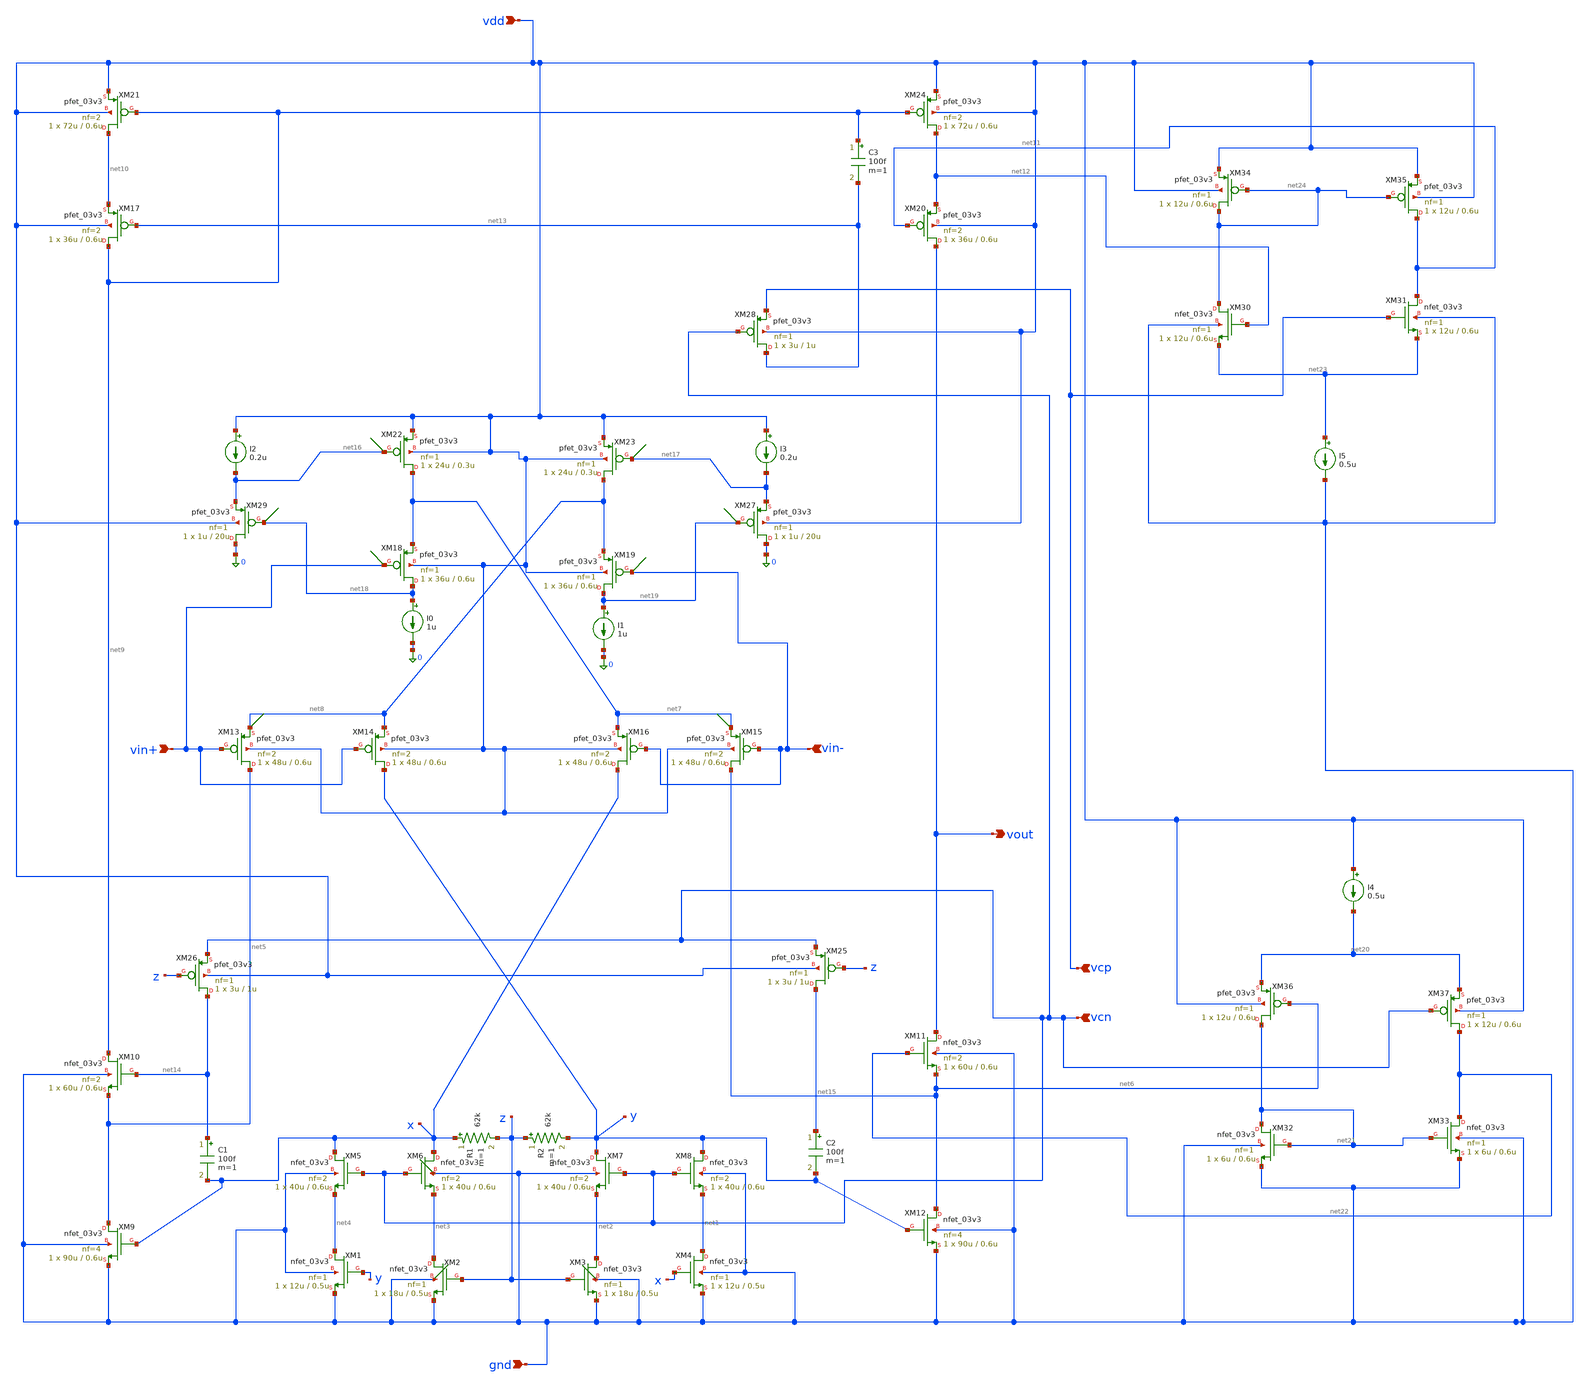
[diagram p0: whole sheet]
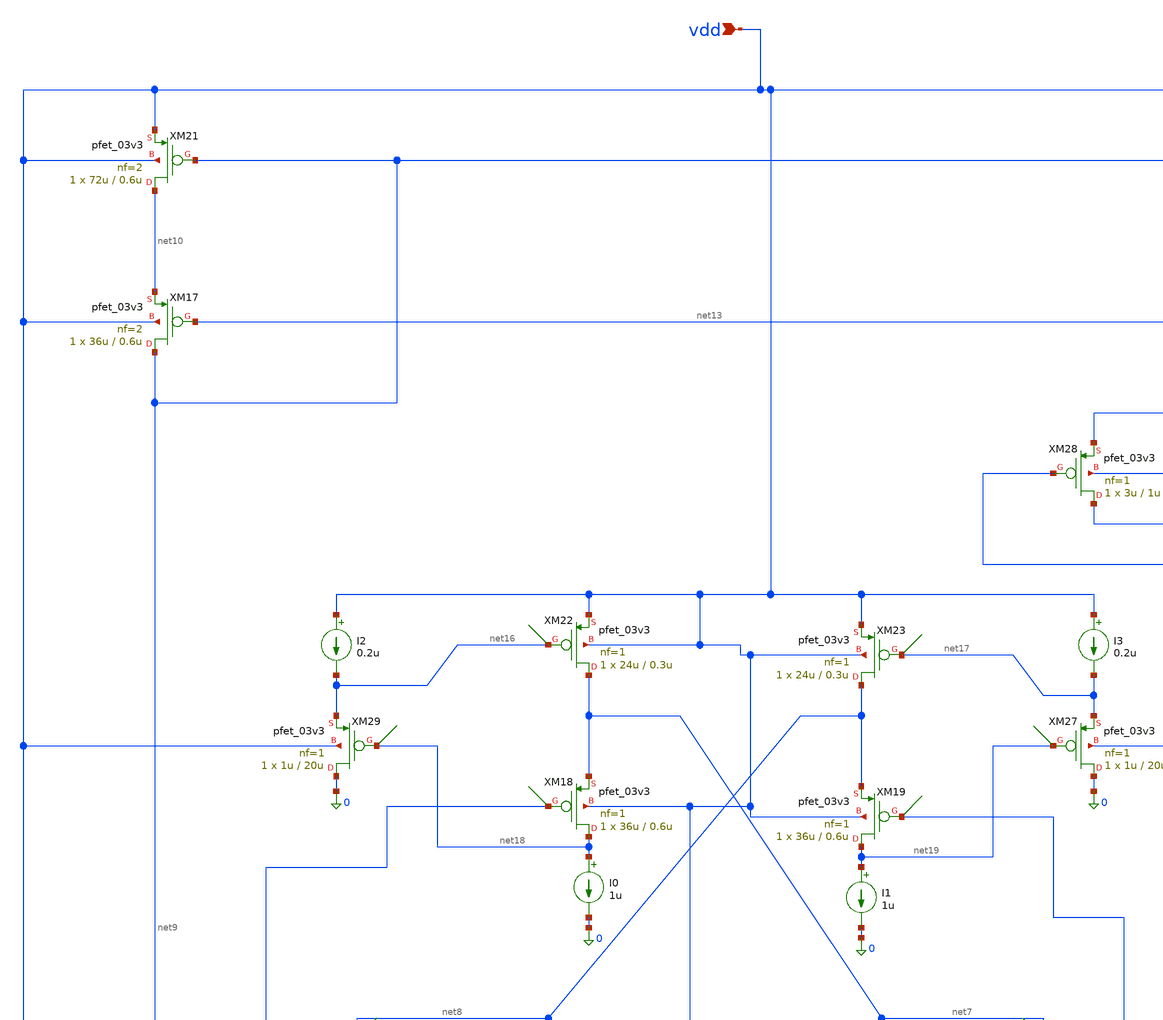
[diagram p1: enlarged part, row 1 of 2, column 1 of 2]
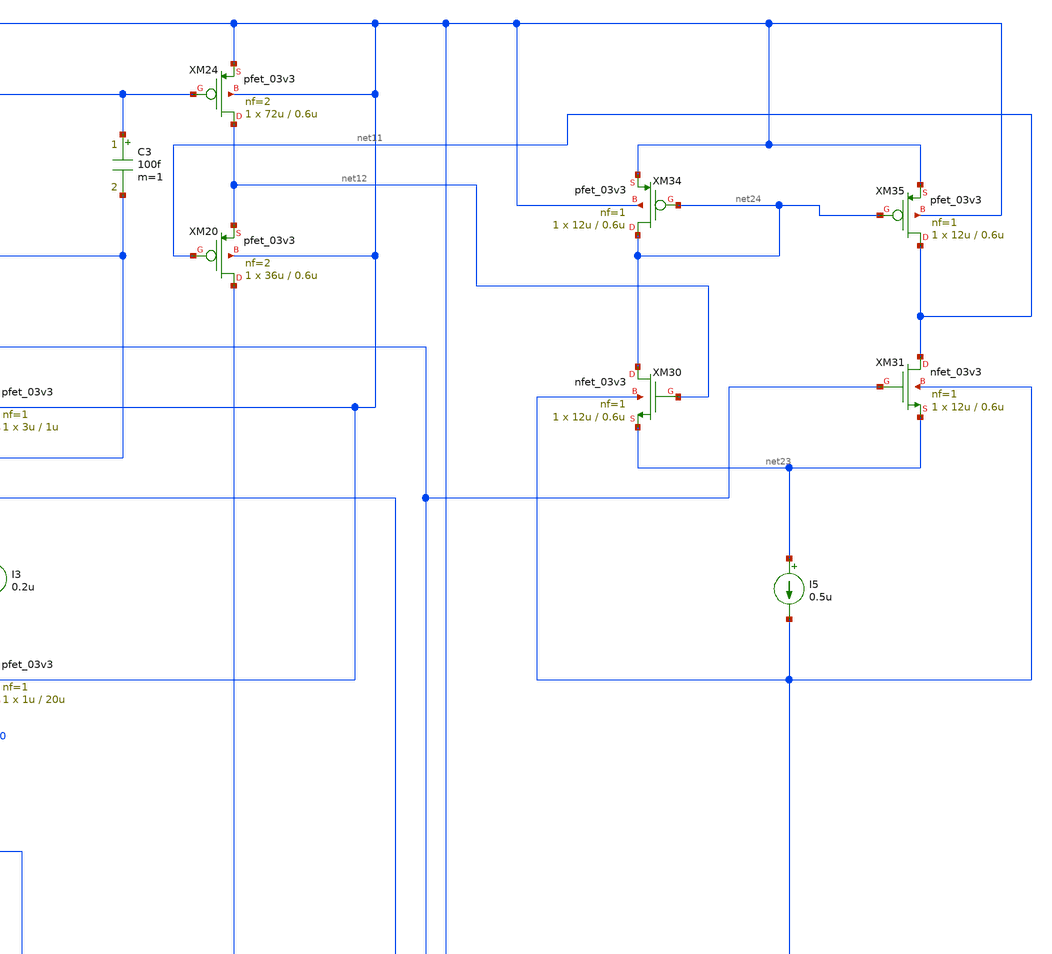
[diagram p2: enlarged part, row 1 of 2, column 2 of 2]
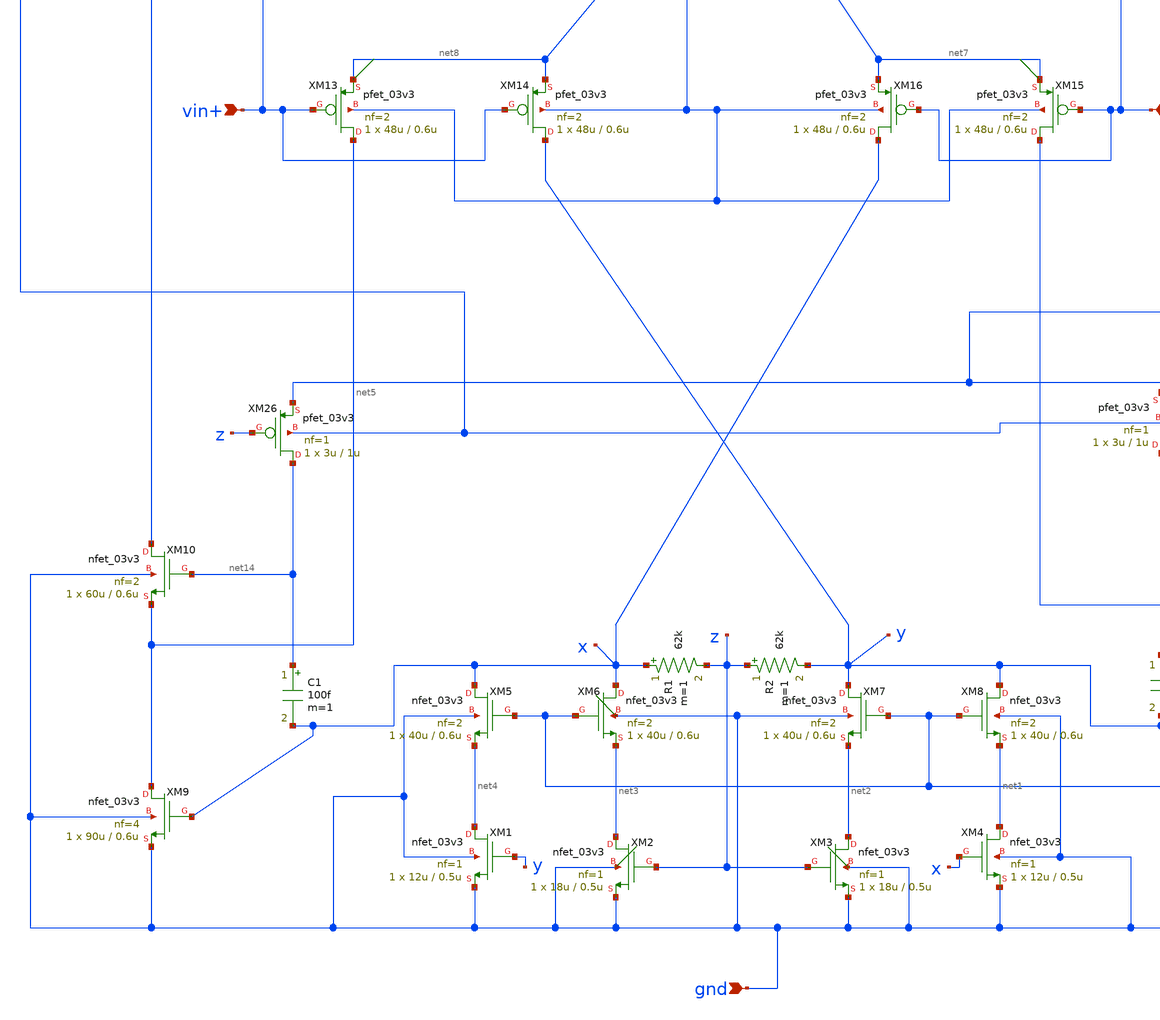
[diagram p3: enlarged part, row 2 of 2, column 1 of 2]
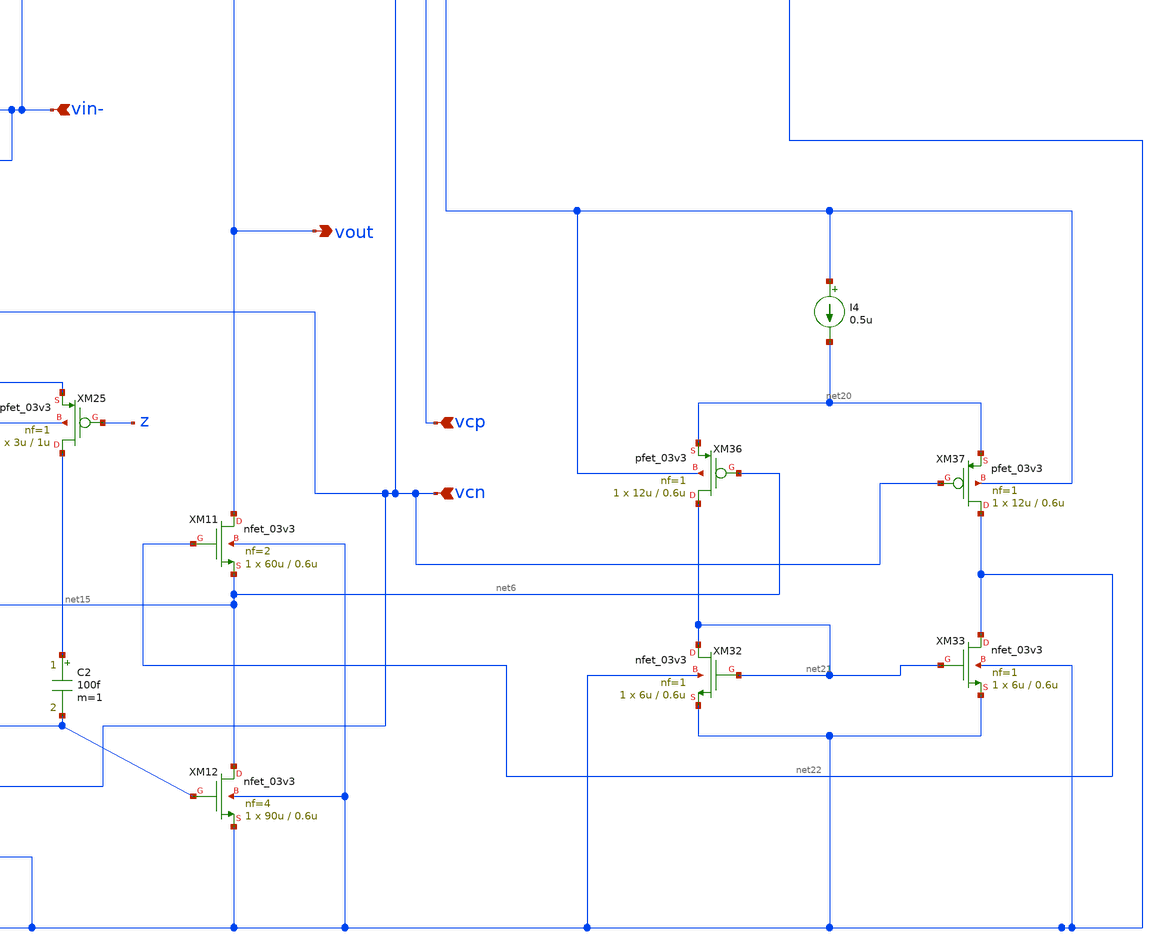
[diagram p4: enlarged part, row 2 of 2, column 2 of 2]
** sch_path: schematic/exp1.sch
**.subckt exp1 gnd vin+ vcp vcn vdd vin- vout
*.ipin gnd
*.ipin vin+
*.ipin vcp
*.ipin vcn
*.ipin vdd
*.ipin vin-
*.opin vout
XM1 net4 y gnd gnd nfet_03v3 L=0.5u W=12u nf=1 ad='int((nf+1)/2) * W/nf * 0.18u' as='int((nf+2)/2) * W/nf * 0.18u'
+ pd='2*int((nf+1)/2) * (W/nf + 0.18u)' ps='2*int((nf+2)/2) * (W/nf + 0.18u)' nrd='0.18u / W' nrs='0.18u / W'
+ sa=0 sb=0 sd=0 m=1
XM2 net3 z gnd gnd nfet_03v3 L=0.5u W=18u nf=1 ad='int((nf+1)/2) * W/nf * 0.18u' as='int((nf+2)/2) * W/nf * 0.18u'
+ pd='2*int((nf+1)/2) * (W/nf + 0.18u)' ps='2*int((nf+2)/2) * (W/nf + 0.18u)' nrd='0.18u / W' nrs='0.18u / W'
+ sa=0 sb=0 sd=0 m=1
XM3 net2 z gnd gnd nfet_03v3 L=0.5u W=18u nf=1 ad='int((nf+1)/2) * W/nf * 0.18u' as='int((nf+2)/2) * W/nf * 0.18u'
+ pd='2*int((nf+1)/2) * (W/nf + 0.18u)' ps='2*int((nf+2)/2) * (W/nf + 0.18u)' nrd='0.18u / W' nrs='0.18u / W'
+ sa=0 sb=0 sd=0 m=1
XM4 net1 x gnd gnd nfet_03v3 L=0.5u W=12u nf=1 ad='int((nf+1)/2) * W/nf * 0.18u' as='int((nf+2)/2) * W/nf * 0.18u'
+ pd='2*int((nf+1)/2) * (W/nf + 0.18u)' ps='2*int((nf+2)/2) * (W/nf + 0.18u)' nrd='0.18u / W' nrs='0.18u / W'
+ sa=0 sb=0 sd=0 m=1
XM5 x vcn net4 gnd nfet_03v3 L=0.6u W=40u nf=2 ad='int((nf+1)/2) * W/nf * 0.18u' as='int((nf+2)/2) * W/nf * 0.18u'
+ pd='2*int((nf+1)/2) * (W/nf + 0.18u)' ps='2*int((nf+2)/2) * (W/nf + 0.18u)' nrd='0.18u / W' nrs='0.18u / W'
+ sa=0 sb=0 sd=0 m=1
XM6 x vcn net3 gnd nfet_03v3 L=0.6u W=40u nf=2 ad='int((nf+1)/2) * W/nf * 0.18u' as='int((nf+2)/2) * W/nf * 0.18u'
+ pd='2*int((nf+1)/2) * (W/nf + 0.18u)' ps='2*int((nf+2)/2) * (W/nf + 0.18u)' nrd='0.18u / W' nrs='0.18u / W'
+ sa=0 sb=0 sd=0 m=1
XM7 y vcn net2 gnd nfet_03v3 L=0.6u W=40u nf=2 ad='int((nf+1)/2) * W/nf * 0.18u' as='int((nf+2)/2) * W/nf * 0.18u'
+ pd='2*int((nf+1)/2) * (W/nf + 0.18u)' ps='2*int((nf+2)/2) * (W/nf + 0.18u)' nrd='0.18u / W' nrs='0.18u / W'
+ sa=0 sb=0 sd=0 m=1
XM8 y vcn net1 gnd nfet_03v3 L=0.6u W=40u nf=2 ad='int((nf+1)/2) * W/nf * 0.18u' as='int((nf+2)/2) * W/nf * 0.18u'
+ pd='2*int((nf+1)/2) * (W/nf + 0.18u)' ps='2*int((nf+2)/2) * (W/nf + 0.18u)' nrd='0.18u / W' nrs='0.18u / W'
+ sa=0 sb=0 sd=0 m=1
XM9 net5 x gnd gnd nfet_03v3 L=0.6u W=90u nf=4 ad='int((nf+1)/2) * W/nf * 0.18u' as='int((nf+2)/2) * W/nf * 0.18u'
+ pd='2*int((nf+1)/2) * (W/nf + 0.18u)' ps='2*int((nf+2)/2) * (W/nf + 0.18u)' nrd='0.18u / W' nrs='0.18u / W'
+ sa=0 sb=0 sd=0 m=1
XM10 net9 net14 net5 gnd nfet_03v3 L=0.6u W=60u nf=2 ad='int((nf+1)/2) * W/nf * 0.18u' as='int((nf+2)/2) * W/nf * 0.18u'
+ pd='2*int((nf+1)/2) * (W/nf + 0.18u)' ps='2*int((nf+2)/2) * (W/nf + 0.18u)' nrd='0.18u / W' nrs='0.18u / W'
+ sa=0 sb=0 sd=0 m=1
XM11 vout net22 net6 gnd nfet_03v3 L=0.6u W=60u nf=2 ad='int((nf+1)/2) * W/nf * 0.18u' as='int((nf+2)/2) * W/nf * 0.18u'
+ pd='2*int((nf+1)/2) * (W/nf + 0.18u)' ps='2*int((nf+2)/2) * (W/nf + 0.18u)' nrd='0.18u / W' nrs='0.18u / W'
+ sa=0 sb=0 sd=0 m=1
XM12 net6 y gnd gnd nfet_03v3 L=0.6u W=90u nf=4 ad='int((nf+1)/2) * W/nf * 0.18u' as='int((nf+2)/2) * W/nf * 0.18u'
+ pd='2*int((nf+1)/2) * (W/nf + 0.18u)' ps='2*int((nf+2)/2) * (W/nf + 0.18u)' nrd='0.18u / W' nrs='0.18u / W'
+ sa=0 sb=0 sd=0 m=1
XM13 net5 vin+ net8 vdd pfet_03v3 L=0.6u W=48u nf=2 ad='int((nf+1)/2) * W/nf * 0.18u' as='int((nf+2)/2) * W/nf * 0.18u'
+ pd='2*int((nf+1)/2) * (W/nf + 0.18u)' ps='2*int((nf+2)/2) * (W/nf + 0.18u)' nrd='0.18u / W' nrs='0.18u / W'
+ sa=0 sb=0 sd=0 m=1
XM14 y vin+ net8 vdd pfet_03v3 L=0.6u W=48u nf=2 ad='int((nf+1)/2) * W/nf * 0.18u' as='int((nf+2)/2) * W/nf * 0.18u'
+ pd='2*int((nf+1)/2) * (W/nf + 0.18u)' ps='2*int((nf+2)/2) * (W/nf + 0.18u)' nrd='0.18u / W' nrs='0.18u / W'
+ sa=0 sb=0 sd=0 m=1
XM15 net6 vin- net7 vdd pfet_03v3 L=0.6u W=48u nf=2 ad='int((nf+1)/2) * W/nf * 0.18u' as='int((nf+2)/2) * W/nf * 0.18u'
+ pd='2*int((nf+1)/2) * (W/nf + 0.18u)' ps='2*int((nf+2)/2) * (W/nf + 0.18u)' nrd='0.18u / W' nrs='0.18u / W'
+ sa=0 sb=0 sd=0 m=1
XM16 x vin- net7 vdd pfet_03v3 L=0.6u W=48u nf=2 ad='int((nf+1)/2) * W/nf * 0.18u' as='int((nf+2)/2) * W/nf * 0.18u'
+ pd='2*int((nf+1)/2) * (W/nf + 0.18u)' ps='2*int((nf+2)/2) * (W/nf + 0.18u)' nrd='0.18u / W' nrs='0.18u / W'
+ sa=0 sb=0 sd=0 m=1
XM17 net9 net13 net10 vdd pfet_03v3 L=0.6u W=36u nf=2 ad='int((nf+1)/2) * W/nf * 0.18u' as='int((nf+2)/2) * W/nf * 0.18u'
+ pd='2*int((nf+1)/2) * (W/nf + 0.18u)' ps='2*int((nf+2)/2) * (W/nf + 0.18u)' nrd='0.18u / W' nrs='0.18u / W'
+ sa=0 sb=0 sd=0 m=1
XM18 net18 vin+ net7 vdd pfet_03v3 L=0.6u W=36u nf=1 ad='int((nf+1)/2) * W/nf * 0.18u' as='int((nf+2)/2) * W/nf * 0.18u'
+ pd='2*int((nf+1)/2) * (W/nf + 0.18u)' ps='2*int((nf+2)/2) * (W/nf + 0.18u)' nrd='0.18u / W' nrs='0.18u / W'
+ sa=0 sb=0 sd=0 m=1
XM19 net19 vin- net8 vdd pfet_03v3 L=0.6u W=36u nf=1 ad='int((nf+1)/2) * W/nf * 0.18u' as='int((nf+2)/2) * W/nf * 0.18u'
+ pd='2*int((nf+1)/2) * (W/nf + 0.18u)' ps='2*int((nf+2)/2) * (W/nf + 0.18u)' nrd='0.18u / W' nrs='0.18u / W'
+ sa=0 sb=0 sd=0 m=1
XM20 vout net11 net12 vdd pfet_03v3 L=0.6u W=36u nf=2 ad='int((nf+1)/2) * W/nf * 0.18u' as='int((nf+2)/2) * W/nf * 0.18u'
+ pd='2*int((nf+1)/2) * (W/nf + 0.18u)' ps='2*int((nf+2)/2) * (W/nf + 0.18u)' nrd='0.18u / W' nrs='0.18u / W'
+ sa=0 sb=0 sd=0 m=1
XM21 net10 net9 vdd vdd pfet_03v3 L=0.6u W=72u nf=2 ad='int((nf+1)/2) * W/nf * 0.18u' as='int((nf+2)/2) * W/nf * 0.18u'
+ pd='2*int((nf+1)/2) * (W/nf + 0.18u)' ps='2*int((nf+2)/2) * (W/nf + 0.18u)' nrd='0.18u / W' nrs='0.18u / W'
+ sa=0 sb=0 sd=0 m=1
XM22 net7 net16 vdd vdd pfet_03v3 L=0.3u W=24u nf=1 ad='int((nf+1)/2) * W/nf * 0.18u' as='int((nf+2)/2) * W/nf * 0.18u'
+ pd='2*int((nf+1)/2) * (W/nf + 0.18u)' ps='2*int((nf+2)/2) * (W/nf + 0.18u)' nrd='0.18u / W' nrs='0.18u / W'
+ sa=0 sb=0 sd=0 m=1
XM23 net8 net17 vdd vdd pfet_03v3 L=0.3u W=24u nf=1 ad='int((nf+1)/2) * W/nf * 0.18u' as='int((nf+2)/2) * W/nf * 0.18u'
+ pd='2*int((nf+1)/2) * (W/nf + 0.18u)' ps='2*int((nf+2)/2) * (W/nf + 0.18u)' nrd='0.18u / W' nrs='0.18u / W'
+ sa=0 sb=0 sd=0 m=1
XM24 net12 net9 vdd vdd pfet_03v3 L=0.6u W=72u nf=2 ad='int((nf+1)/2) * W/nf * 0.18u' as='int((nf+2)/2) * W/nf * 0.18u'
+ pd='2*int((nf+1)/2) * (W/nf + 0.18u)' ps='2*int((nf+2)/2) * (W/nf + 0.18u)' nrd='0.18u / W' nrs='0.18u / W'
+ sa=0 sb=0 sd=0 m=1
XM25 net15 z vcn vdd pfet_03v3 L=1u W=3u nf=1 ad='int((nf+1)/2) * W/nf * 0.18u' as='int((nf+2)/2) * W/nf * 0.18u'
+ pd='2*int((nf+1)/2) * (W/nf + 0.18u)' ps='2*int((nf+2)/2) * (W/nf + 0.18u)' nrd='0.18u / W' nrs='0.18u / W'
+ sa=0 sb=0 sd=0 m=1
XM26 net14 z vcn vdd pfet_03v3 L=1u W=3u nf=1 ad='int((nf+1)/2) * W/nf * 0.18u' as='int((nf+2)/2) * W/nf * 0.18u'
+ pd='2*int((nf+1)/2) * (W/nf + 0.18u)' ps='2*int((nf+2)/2) * (W/nf + 0.18u)' nrd='0.18u / W' nrs='0.18u / W'
+ sa=0 sb=0 sd=0 m=1
XM27 0 net19 net17 vdd pfet_03v3 L=20u W=1u nf=1 ad='int((nf+1)/2) * W/nf * 0.18u' as='int((nf+2)/2) * W/nf * 0.18u'
+ pd='2*int((nf+1)/2) * (W/nf + 0.18u)' ps='2*int((nf+2)/2) * (W/nf + 0.18u)' nrd='0.18u / W' nrs='0.18u / W'
+ sa=0 sb=0 sd=0 m=1
XM28 net13 vcn vcp vdd pfet_03v3 L=1u W=3u nf=1 ad='int((nf+1)/2) * W/nf * 0.18u' as='int((nf+2)/2) * W/nf * 0.18u'
+ pd='2*int((nf+1)/2) * (W/nf + 0.18u)' ps='2*int((nf+2)/2) * (W/nf + 0.18u)' nrd='0.18u / W' nrs='0.18u / W'
+ sa=0 sb=0 sd=0 m=1
XM29 0 net18 net16 vdd pfet_03v3 L=20u W=1u nf=1 ad='int((nf+1)/2) * W/nf * 0.18u' as='int((nf+2)/2) * W/nf * 0.18u'
+ pd='2*int((nf+1)/2) * (W/nf + 0.18u)' ps='2*int((nf+2)/2) * (W/nf + 0.18u)' nrd='0.18u / W' nrs='0.18u / W'
+ sa=0 sb=0 sd=0 m=1
I0 net18 0 1u
I1 net19 0 1u
I2 vdd net16 0.2u
I3 vdd net17 0.2u
C1 net14 x 100f m=1
C2 net15 y 100f m=1
C3 net9 net13 100f m=1
R1 x z 62k m=1
R2 z y 62k m=1
XM30 net24 net12 net23 gnd nfet_03v3 L=0.6u W=12u nf=1 ad='int((nf+1)/2) * W/nf * 0.18u' as='int((nf+2)/2) * W/nf * 0.18u'
+ pd='2*int((nf+1)/2) * (W/nf + 0.18u)' ps='2*int((nf+2)/2) * (W/nf + 0.18u)' nrd='0.18u / W' nrs='0.18u / W'
+ sa=0 sb=0 sd=0 m=1
XM31 net11 vcp net23 gnd nfet_03v3 L=0.6u W=12u nf=1 ad='int((nf+1)/2) * W/nf * 0.18u' as='int((nf+2)/2) * W/nf * 0.18u'
+ pd='2*int((nf+1)/2) * (W/nf + 0.18u)' ps='2*int((nf+2)/2) * (W/nf + 0.18u)' nrd='0.18u / W' nrs='0.18u / W'
+ sa=0 sb=0 sd=0 m=1
XM32 net21 net21 gnd gnd nfet_03v3 L=0.6u W=6u nf=1 ad='int((nf+1)/2) * W/nf * 0.18u' as='int((nf+2)/2) * W/nf * 0.18u'
+ pd='2*int((nf+1)/2) * (W/nf + 0.18u)' ps='2*int((nf+2)/2) * (W/nf + 0.18u)' nrd='0.18u / W' nrs='0.18u / W'
+ sa=0 sb=0 sd=0 m=1
XM33 net22 net21 gnd gnd nfet_03v3 L=0.6u W=6u nf=1 ad='int((nf+1)/2) * W/nf * 0.18u' as='int((nf+2)/2) * W/nf * 0.18u'
+ pd='2*int((nf+1)/2) * (W/nf + 0.18u)' ps='2*int((nf+2)/2) * (W/nf + 0.18u)' nrd='0.18u / W' nrs='0.18u / W'
+ sa=0 sb=0 sd=0 m=1
XM34 net24 net24 vdd vdd pfet_03v3 L=0.6u W=12u nf=1 ad='int((nf+1)/2) * W/nf * 0.18u' as='int((nf+2)/2) * W/nf * 0.18u'
+ pd='2*int((nf+1)/2) * (W/nf + 0.18u)' ps='2*int((nf+2)/2) * (W/nf + 0.18u)' nrd='0.18u / W' nrs='0.18u / W'
+ sa=0 sb=0 sd=0 m=1
XM35 net11 net24 vdd vdd pfet_03v3 L=0.6u W=12u nf=1 ad='int((nf+1)/2) * W/nf * 0.18u' as='int((nf+2)/2) * W/nf * 0.18u'
+ pd='2*int((nf+1)/2) * (W/nf + 0.18u)' ps='2*int((nf+2)/2) * (W/nf + 0.18u)' nrd='0.18u / W' nrs='0.18u / W'
+ sa=0 sb=0 sd=0 m=1
XM36 net21 net6 net20 vdd pfet_03v3 L=0.6u W=12u nf=1 ad='int((nf+1)/2) * W/nf * 0.18u' as='int((nf+2)/2) * W/nf * 0.18u'
+ pd='2*int((nf+1)/2) * (W/nf + 0.18u)' ps='2*int((nf+2)/2) * (W/nf + 0.18u)' nrd='0.18u / W' nrs='0.18u / W'
+ sa=0 sb=0 sd=0 m=1
XM37 net22 vcn net20 vdd pfet_03v3 L=0.6u W=12u nf=1 ad='int((nf+1)/2) * W/nf * 0.18u' as='int((nf+2)/2) * W/nf * 0.18u'
+ pd='2*int((nf+1)/2) * (W/nf + 0.18u)' ps='2*int((nf+2)/2) * (W/nf + 0.18u)' nrd='0.18u / W' nrs='0.18u / W'
+ sa=0 sb=0 sd=0 m=1
I4 vdd net20 0.5u
I5 net23 gnd 0.5u
**.ends
.end
